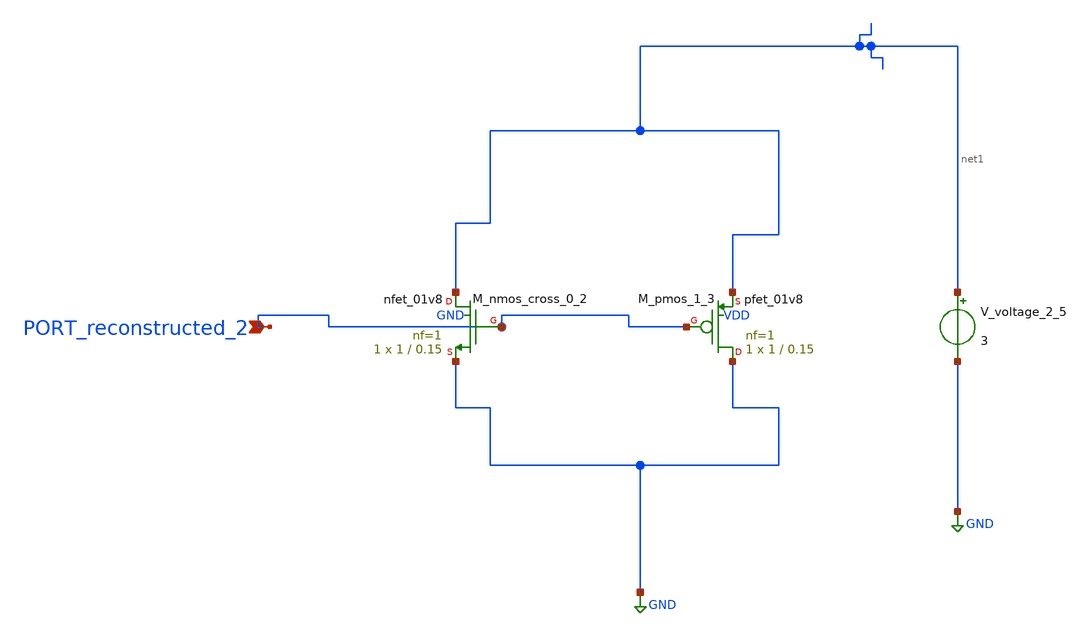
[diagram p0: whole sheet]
** sch_path: schematics/AMSNet/60.sch
**.subckt 60 PORT_reconstructed_2
*.ipin PORT_reconstructed_2
XM_nmos_cross_0_2 net1 PORT_reconstructed_2 GND GND sky130_fd_pr__nfet_01v8 L=0.15 W=1 nf=1 ad='int((1 + 1)/2) * 1 / 1 * 0.29'
+ as='int((1 + 2)/2) * 1 / 1 * 0.29' pd='2*int((1 + 1)/2) * (1 / 1 + 0.29)' ps='2*int((1 + 2)/2) * (1 / 1 + 0.29)'
+ nrd='0.29 / 1 ' nrs='0.29 / 1 ' sa=0 sb=0 sd=0 mult=1 m=1
XM_pmos_1_3 GND PORT_reconstructed_2 net1 VDD sky130_fd_pr__pfet_01v8 L=0.15 W=1 nf=1 ad='int((1 + 1)/2) * 1 / 1 * 0.29'
+ as='int((1 + 2)/2) * 1 / 1 * 0.29' pd='2*int((1 + 1)/2) * (1 / 1 + 0.29)' ps='2*int((1 + 2)/2) * (1 / 1 + 0.29)'
+ nrd='0.29 / 1 ' nrs='0.29 / 1 ' sa=0 sb=0 sd=0 mult=1 m=1
V_voltage_2_5 net1 GND 3
**.ends
.GLOBAL GND
.end
